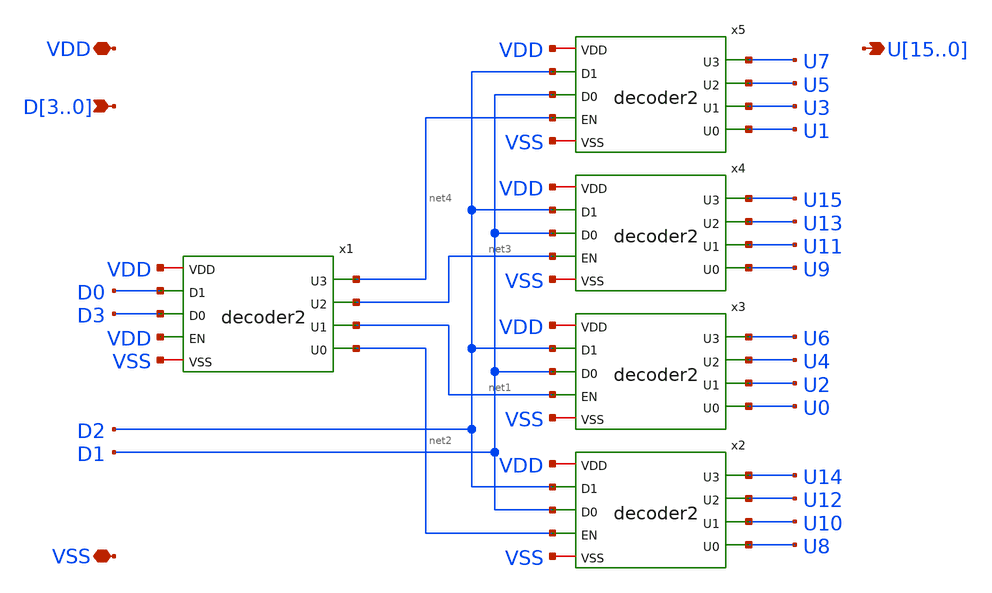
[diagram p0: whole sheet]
** sch_path: xschem/decoder4_signed.sch
**.subckt decoder4_signed VDD VSS U15,U14,U13,U12,U11,U10,U9,U8,U7,U6,U5,U4,U3,U2,U1,U0 D3,D2,D1,D0
*.iopin VDD
*.iopin VSS
*.opin U15,U14,U13,U12,U11,U10,U9,U8,U7,U6,U5,U4,U3,U2,U1,U0
*.ipin D3,D2,D1,D0
x1 VDD D0 D3 net4 net3 net1 net2 VSS VDD decoder2
x2 VDD D2 D1 U14 U12 U10 U8 VSS net2 decoder2
x3 VDD D2 D1 U6 U4 U2 U0 VSS net1 decoder2
x4 VDD D2 D1 U15 U13 U11 U9 VSS net3 decoder2
x5 VDD D2 D1 U7 U5 U3 U1 VSS net4 decoder2
**.ends

* expanding   symbol:  decoder2.sym # of pins=9
** sym_path: xschem/decoder2.sym
** sch_path: xschem/decoder2.sch
.subckt decoder2 VDD D1 D0 U3 U2 U1 U0 VSS EN
*.iopin VDD
*.iopin VSS
*.ipin D0
*.ipin D1
*.opin U0
*.opin U1
*.opin U2
*.opin U3
*.ipin EN
x6 VDD net5 net4 U0 net3 VSS nor3
x7 VDD net5 net1 U1 net3 VSS nor3
x8 VDD net2 net4 U2 net3 VSS nor3
x9 VDD net2 net1 U3 net3 VSS nor3
x1 VDD EN net3 VSS inverter
x2 VDD D0 net1 VSS inverter
x3 VDD net1 net4 VSS inverter
x4 VDD D1 net2 VSS inverter
x5 VDD net2 net5 VSS inverter
.ends


* expanding   symbol:  nor3.sym # of pins=6
** sym_path: xschem/nor3.sym
** sch_path: xschem/nor3.sch
.subckt nor3 VDD A B OUT C VSS
*.iopin VSS
*.iopin VDD
*.ipin B
*.ipin A
*.ipin C
*.opin OUT
XM2 OUT B VSS VSS sky130_fd_pr__nfet_g5v0d10v5 L=0.5 W=0.65 nf=1 ad='int((1 + 1)/2) * 0.65 / 1 * 0.29'
+ as='int((1 + 2)/2) * 0.65 / 1 * 0.29' pd='2*int((1 + 1)/2) * (0.65 / 1 + 0.29)' ps='2*int((1 + 2)/2) * (0.65 / 1 + 0.29)'
+ nrd='0.29 / 0.65 ' nrs='0.29 / 0.65 ' sa=0 sb=0 sd=0 mult=1 m=1
XM1 OUT A VSS VSS sky130_fd_pr__nfet_g5v0d10v5 L=0.5 W=0.65 nf=1 ad='int((1 + 1)/2) * 0.65 / 1 * 0.29'
+ as='int((1 + 2)/2) * 0.65 / 1 * 0.29' pd='2*int((1 + 1)/2) * (0.65 / 1 + 0.29)' ps='2*int((1 + 2)/2) * (0.65 / 1 + 0.29)'
+ nrd='0.29 / 0.65 ' nrs='0.29 / 0.65 ' sa=0 sb=0 sd=0 mult=1 m=1
XM4 net1 A VDD VDD sky130_fd_pr__pfet_g5v0d10v5 L=0.5 W=1 nf=1 ad='int((1 + 1)/2) * 1 / 1 * 0.29' as='int((1 + 2)/2) * 1 / 1 * 0.29'
+ pd='2*int((1 + 1)/2) * (1 / 1 + 0.29)' ps='2*int((1 + 2)/2) * (1 / 1 + 0.29)' nrd='0.29 / 1 ' nrs='0.29 / 1 '
+ sa=0 sb=0 sd=0 mult=1 m=1
XM3 OUT C VSS VSS sky130_fd_pr__nfet_g5v0d10v5 L=0.5 W=0.65 nf=1 ad='int((1 + 1)/2) * 0.65 / 1 * 0.29'
+ as='int((1 + 2)/2) * 0.65 / 1 * 0.29' pd='2*int((1 + 1)/2) * (0.65 / 1 + 0.29)' ps='2*int((1 + 2)/2) * (0.65 / 1 + 0.29)'
+ nrd='0.29 / 0.65 ' nrs='0.29 / 0.65 ' sa=0 sb=0 sd=0 mult=1 m=1
XM5 net2 B net1 VDD sky130_fd_pr__pfet_g5v0d10v5 L=0.5 W=1 nf=1 ad='int((1 + 1)/2) * 1 / 1 * 0.29' as='int((1 + 2)/2) * 1 / 1 * 0.29'
+ pd='2*int((1 + 1)/2) * (1 / 1 + 0.29)' ps='2*int((1 + 2)/2) * (1 / 1 + 0.29)' nrd='0.29 / 1 ' nrs='0.29 / 1 '
+ sa=0 sb=0 sd=0 mult=1 m=1
XM6 OUT C net2 VDD sky130_fd_pr__pfet_g5v0d10v5 L=0.5 W=1 nf=1 ad='int((1 + 1)/2) * 1 / 1 * 0.29' as='int((1 + 2)/2) * 1 / 1 * 0.29'
+ pd='2*int((1 + 1)/2) * (1 / 1 + 0.29)' ps='2*int((1 + 2)/2) * (1 / 1 + 0.29)' nrd='0.29 / 1 ' nrs='0.29 / 1 '
+ sa=0 sb=0 sd=0 mult=1 m=1
.ends


* expanding   symbol:  inverter.sym # of pins=4
** sym_path: xschem/inverter.sym
** sch_path: xschem/inverter.sch
.subckt inverter VDD IN OUT VSS
*.iopin VSS
*.iopin VDD
*.ipin IN
*.opin OUT
XM1 OUT IN VSS VSS sky130_fd_pr__nfet_g5v0d10v5 L=0.5 W=0.65 nf=1 ad='int((1 + 1)/2) * 0.65 / 1 * 0.29'
+ as='int((1 + 2)/2) * 0.65 / 1 * 0.29' pd='2*int((1 + 1)/2) * (0.65 / 1 + 0.29)' ps='2*int((1 + 2)/2) * (0.65 / 1 + 0.29)'
+ nrd='0.29 / 0.65 ' nrs='0.29 / 0.65 ' sa=0 sb=0 sd=0 mult=1 m=1
XM2 OUT IN VDD VDD sky130_fd_pr__pfet_g5v0d10v5 L=0.5 W=1 nf=1 ad='int((1 + 1)/2) * 1 / 1 * 0.29' as='int((1 + 2)/2) * 1 / 1 * 0.29'
+ pd='2*int((1 + 1)/2) * (1 / 1 + 0.29)' ps='2*int((1 + 2)/2) * (1 / 1 + 0.29)' nrd='0.29 / 1 ' nrs='0.29 / 1 '
+ sa=0 sb=0 sd=0 mult=1 m=1
.ends

.end
